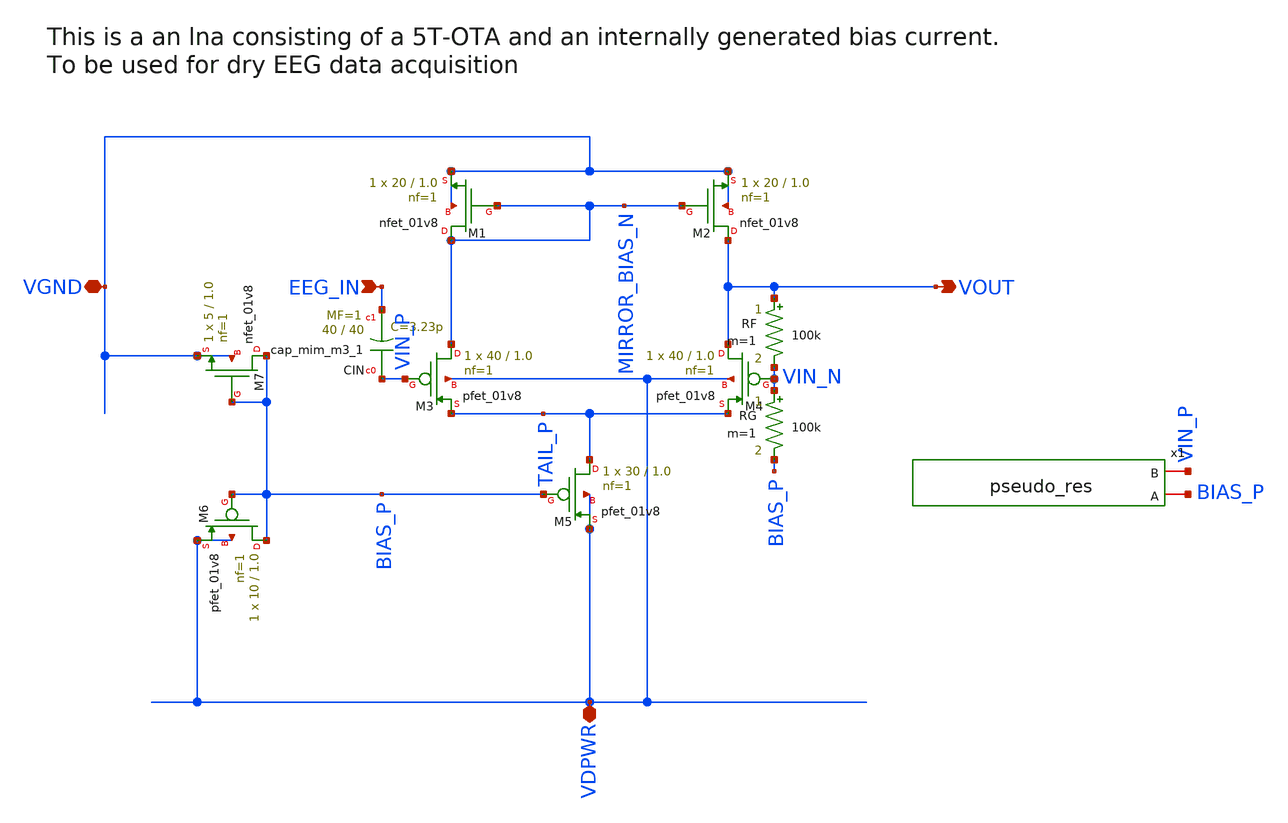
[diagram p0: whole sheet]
** sch_path: xschem/eeg_lna.sch
**.subckt eeg_lna VGND EEG_IN VDPWR VOUT
*.iopin VGND
*.ipin EEG_IN
*.iopin VDPWR
*.opin VOUT
XM1 MIRROR_BIAS_N MIRROR_BIAS_N VGND VGND sky130_fd_pr__nfet_01v8 L=1.0 W=20 nf=1 ad='int((1 + 1)/2) * 20 / 1 * 0.29'
+ as='int((1 + 2)/2) * 20 / 1 * 0.29' pd='2*int((1 + 1)/2) * (20 / 1 + 0.29)' ps='2*int((1 + 2)/2) * (20 / 1 + 0.29)'
+ nrd='0.29 / 20 ' nrs='0.29 / 20 ' sa=0 sb=0 sd=0 mult=1 m=1
XM2 VOUT MIRROR_BIAS_N VGND VGND sky130_fd_pr__nfet_01v8 L=1.0 W=20 nf=1 ad='int((1 + 1)/2) * 20 / 1 * 0.29'
+ as='int((1 + 2)/2) * 20 / 1 * 0.29' pd='2*int((1 + 1)/2) * (20 / 1 + 0.29)' ps='2*int((1 + 2)/2) * (20 / 1 + 0.29)'
+ nrd='0.29 / 20 ' nrs='0.29 / 20 ' sa=0 sb=0 sd=0 mult=1 m=1
XM3 MIRROR_BIAS_N VIN_P TAIL_P VDPWR sky130_fd_pr__pfet_01v8 L=1.0 W=40 nf=1 ad='int((1 + 1)/2) * 40 / 1 * 0.29'
+ as='int((1 + 2)/2) * 40 / 1 * 0.29' pd='2*int((1 + 1)/2) * (40 / 1 + 0.29)' ps='2*int((1 + 2)/2) * (40 / 1 + 0.29)'
+ nrd='0.29 / 40 ' nrs='0.29 / 40 ' sa=0 sb=0 sd=0 mult=1 m=1
XM4 VOUT VIN_N TAIL_P VDPWR sky130_fd_pr__pfet_01v8 L=1.0 W=40 nf=1 ad='int((1 + 1)/2) * 40 / 1 * 0.29'
+ as='int((1 + 2)/2) * 40 / 1 * 0.29' pd='2*int((1 + 1)/2) * (40 / 1 + 0.29)' ps='2*int((1 + 2)/2) * (40 / 1 + 0.29)'
+ nrd='0.29 / 40 ' nrs='0.29 / 40 ' sa=0 sb=0 sd=0 mult=1 m=1
XM5 TAIL_P BIAS_P VDPWR VDPWR sky130_fd_pr__pfet_01v8 L=1.0 W=30 nf=1 ad='int((1 + 1)/2) * 30 / 1 * 0.29'
+ as='int((1 + 2)/2) * 30 / 1 * 0.29' pd='2*int((1 + 1)/2) * (30 / 1 + 0.29)' ps='2*int((1 + 2)/2) * (30 / 1 + 0.29)'
+ nrd='0.29 / 30 ' nrs='0.29 / 30 ' sa=0 sb=0 sd=0 mult=1 m=1
XM6 BIAS_P BIAS_P VDPWR VDPWR sky130_fd_pr__pfet_01v8 L=1.0 W=10 nf=1 ad='int((1 + 1)/2) * 10 / 1 * 0.29'
+ as='int((1 + 2)/2) * 10 / 1 * 0.29' pd='2*int((1 + 1)/2) * (10 / 1 + 0.29)' ps='2*int((1 + 2)/2) * (10 / 1 + 0.29)'
+ nrd='0.29 / 10 ' nrs='0.29 / 10 ' sa=0 sb=0 sd=0 mult=1 m=1
XM7 BIAS_P BIAS_P VGND VGND sky130_fd_pr__nfet_01v8 L=1.0 W=5 nf=1 ad='int((1 + 1)/2) * 5 / 1 * 0.29'
+ as='int((1 + 2)/2) * 5 / 1 * 0.29' pd='2*int((1 + 1)/2) * (5 / 1 + 0.29)' ps='2*int((1 + 2)/2) * (5 / 1 + 0.29)'
+ nrd='0.29 / 5 ' nrs='0.29 / 5 ' sa=0 sb=0 sd=0 mult=1 m=1
XCIN VIN_P EEG_IN sky130_fd_pr__cap_mim_m3_1 W=40 L=40 MF=1 m=1
RF VOUT VIN_N 100k m=1
RG VIN_N BIAS_P 100k m=1
x1 VIN_P BIAS_P pseudo_res
**.ends

* expanding   symbol:  pseudo_res.sym # of pins=2
** sym_path: xschem/pseudo_res.sym
** sch_path: xschem/pseudo_res.sch
.subckt pseudo_res B A
*.iopin A
*.iopin B
XM1 B B A A sky130_fd_pr__pfet_01v8 L=10 W=0.42 nf=1 ad='int((1 + 1)/2) * 0.42 / 1 * 0.29' as='int((1 + 2)/2) * 0.42 / 1 * 0.29'
+ pd='2*int((1 + 1)/2) * (0.42 / 1 + 0.29)' ps='2*int((1 + 2)/2) * (0.42 / 1 + 0.29)' nrd='0.29 / 0.42 '
+ nrs='0.29 / 0.42 ' sa=0 sb=0 sd=0 mult=1 m=1
XM2 A A B B sky130_fd_pr__pfet_01v8 L=10 W=0.42 nf=1 ad='int((1 + 1)/2) * 0.42 / 1 * 0.29' as='int((1 + 2)/2) * 0.42 / 1 * 0.29'
+ pd='2*int((1 + 1)/2) * (0.42 / 1 + 0.29)' ps='2*int((1 + 2)/2) * (0.42 / 1 + 0.29)' nrd='0.29 / 0.42 '
+ nrs='0.29 / 0.42 ' sa=0 sb=0 sd=0 mult=1 m=1
.ends

.end
